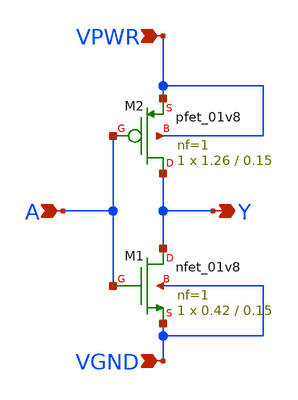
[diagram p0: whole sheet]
** sch_path: inverter/phase1/xschem/INV.sch
**.subckt INV Y A VPWR VGND
*.opin Y
*.ipin A
*.ipin VPWR
*.ipin VGND
XM1 Y A VGND VGND sky130_fd_pr__nfet_01v8 L=0.15 W=0.42 nf=1 ad='int((1 + 1)/2) * 0.42 / 1 * 0.29' as='int((1 + 2)/2) * 0.42 / 1 * 0.29'
+ pd='2*int((1 + 1)/2) * (0.42 / 1 + 0.29)' ps='2*int((1 + 2)/2) * (0.42 / 1 + 0.29)' nrd='0.29 / 0.42 '
+ nrs='0.29 / 0.42 ' sa=0 sb=0 sd=0 mult=1 m=1
XM2 Y A VPWR VPWR sky130_fd_pr__pfet_01v8 L=0.15 W=1.26 nf=1 ad='int((nf+1)/2) * W/nf * 0.29' as='int((nf+2)/2) * W/nf * 0.29'
+ pd='2*int((nf+1)/2) * (W/nf + 0.29)' ps='2*int((nf+2)/2) * (W/nf + 0.29)' nrd='0.29 / W' nrs='0.29 / W'
+ sa=0 sb=0 sd=0 mult=1 m=1
**.ends
.end
